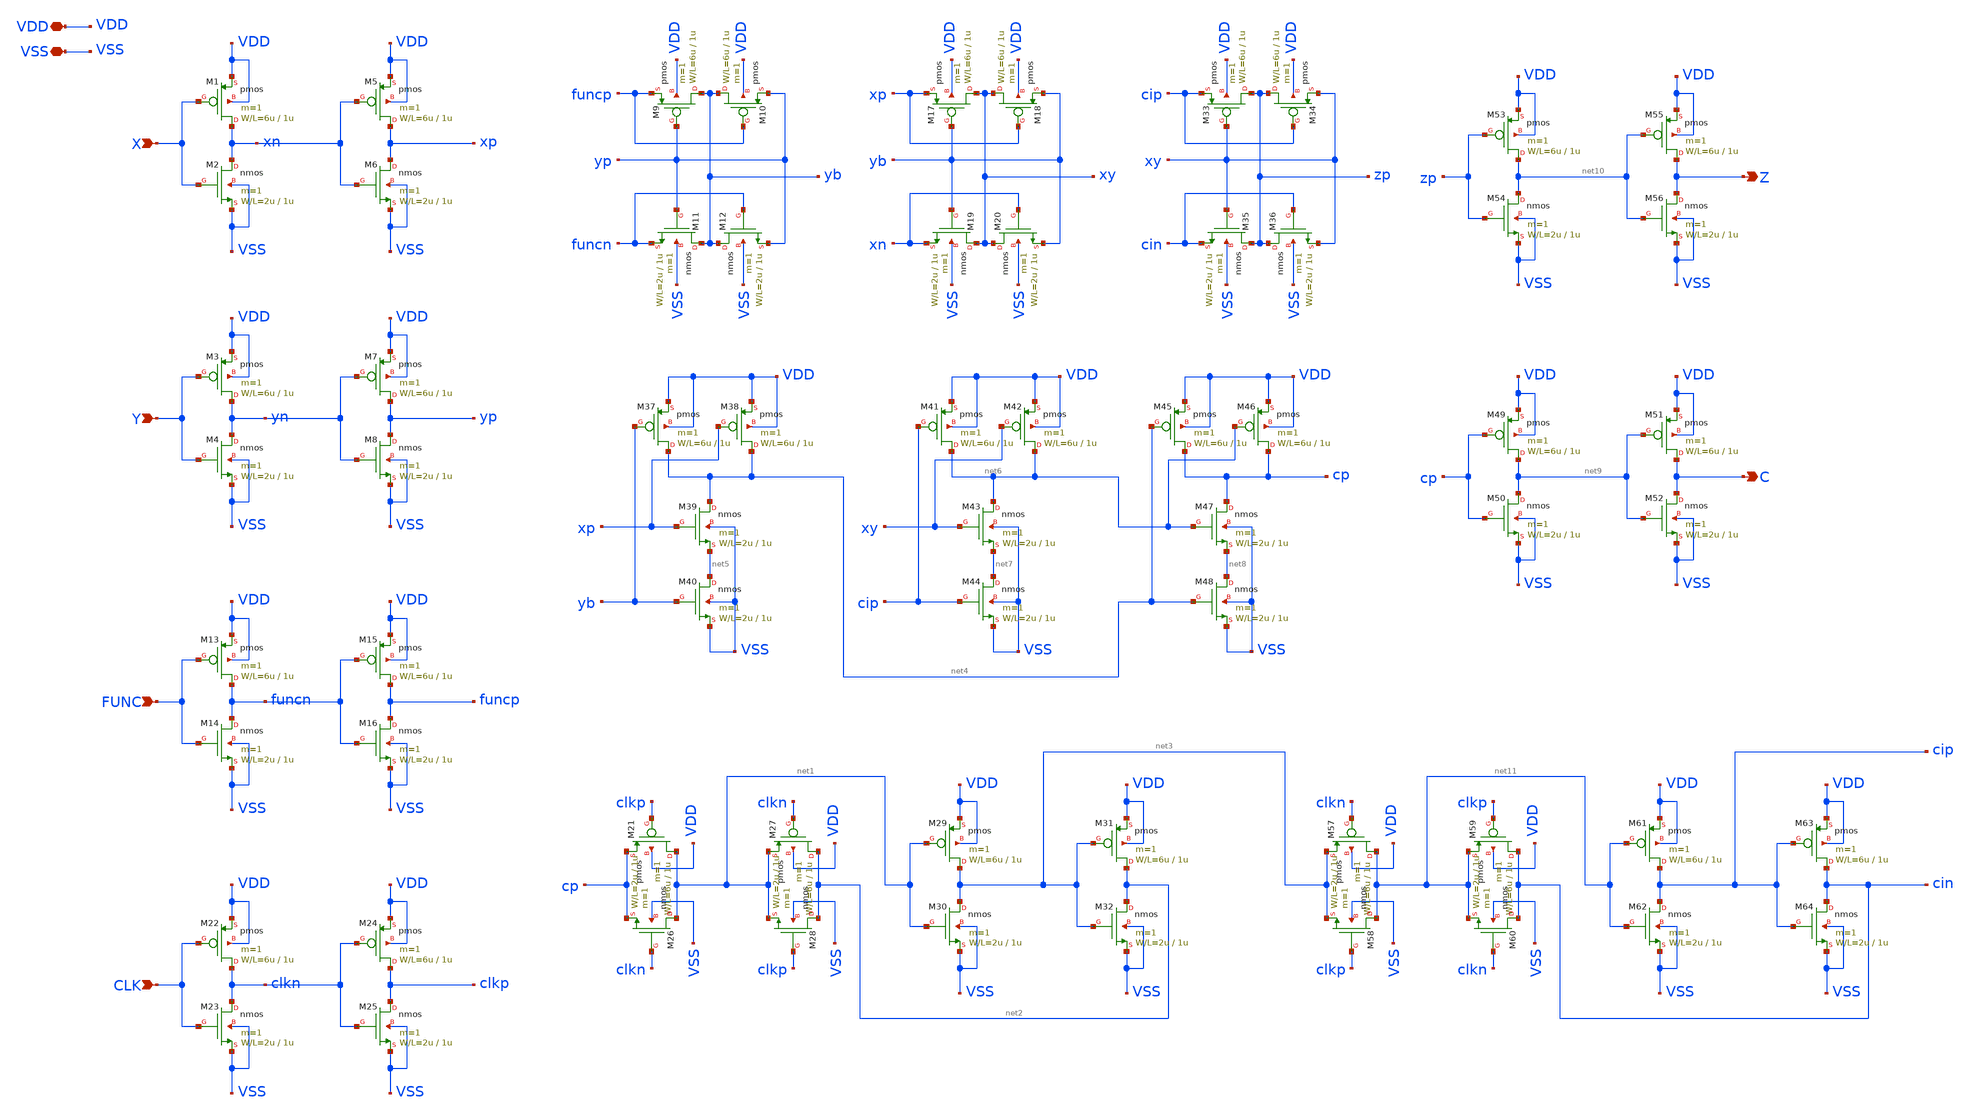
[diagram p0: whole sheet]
** sch_path: member_project/sanken/yamazaki/infinite_ALU/infinite_ALU.sch
**.subckt infinite_ALU X Y FUNC CLK Z C VDD VSS
*.ipin X
*.ipin Y
*.ipin FUNC
*.ipin CLK
*.opin Z
*.opin C
*.iopin VDD
*.iopin VSS
M1 xn X VDD VDD pmos L=1u W=6u m=1
M2 xn X VSS VSS nmos L=1u W=2u m=1
M3 yn Y VDD VDD pmos L=1u W=6u m=1
M4 yn Y VSS VSS nmos L=1u W=2u m=1
M5 xp xn VDD VDD pmos L=1u W=6u m=1
M6 xp xn VSS VSS nmos L=1u W=2u m=1
M7 yp yn VDD VDD pmos L=1u W=6u m=1
M8 yp yn VSS VSS nmos L=1u W=2u m=1
M9 yb yp funcp VDD pmos L=1u W=6u m=1
M10 yb funcp yp VDD pmos L=1u W=6u m=1
M11 yb yp funcn VSS nmos L=1u W=2u m=1
M12 yb funcn yp VSS nmos L=1u W=2u m=1
M13 funcn FUNC VDD VDD pmos L=1u W=6u m=1
M14 funcn FUNC VSS VSS nmos L=1u W=2u m=1
M15 funcp funcn VDD VDD pmos L=1u W=6u m=1
M16 funcp funcn VSS VSS nmos L=1u W=2u m=1
M17 xy yb xp VDD pmos L=1u W=6u m=1
M18 xy xp yb VDD pmos L=1u W=6u m=1
M19 xy yb xn VSS nmos L=1u W=2u m=1
M20 xy xn yb VSS nmos L=1u W=2u m=1
M21 net1 clkp cp VDD pmos L=1u W=6u m=1
M22 clkn CLK VDD VDD pmos L=1u W=6u m=1
M23 clkn CLK VSS VSS nmos L=1u W=2u m=1
M24 clkp clkn VDD VDD pmos L=1u W=6u m=1
M25 clkp clkn VSS VSS nmos L=1u W=2u m=1
M26 net1 clkn cp VSS nmos L=1u W=2u m=1
M27 net2 clkn net1 VDD pmos L=1u W=6u m=1
M28 net2 clkp net1 VSS nmos L=1u W=2u m=1
M29 net3 net1 VDD VDD pmos L=1u W=6u m=1
M30 net3 net1 VSS VSS nmos L=1u W=2u m=1
M31 net2 net3 VDD VDD pmos L=1u W=6u m=1
M32 net2 net3 VSS VSS nmos L=1u W=2u m=1
M33 zp xy cip VDD pmos L=1u W=6u m=1
M34 zp cip xy VDD pmos L=1u W=6u m=1
M35 zp xy cin VSS nmos L=1u W=2u m=1
M36 zp cin xy VSS nmos L=1u W=2u m=1
M37 net4 yb VDD VDD pmos L=1u W=6u m=1
M38 net4 xp VDD VDD pmos L=1u W=6u m=1
M39 net4 xp net5 VSS nmos L=1u W=2u m=1
M40 net5 yb VSS VSS nmos L=1u W=2u m=1
M41 net6 cip VDD VDD pmos L=1u W=6u m=1
M42 net6 xy VDD VDD pmos L=1u W=6u m=1
M43 net6 xy net7 VSS nmos L=1u W=2u m=1
M44 net7 cip VSS VSS nmos L=1u W=2u m=1
M45 cp net4 VDD VDD pmos L=1u W=6u m=1
M46 cp net6 VDD VDD pmos L=1u W=6u m=1
M47 cp net6 net8 VSS nmos L=1u W=2u m=1
M48 net8 net4 VSS VSS nmos L=1u W=2u m=1
M49 net9 cp VDD VDD pmos L=1u W=6u m=1
M50 net9 cp VSS VSS nmos L=1u W=2u m=1
M51 C net9 VDD VDD pmos L=1u W=6u m=1
M52 C net9 VSS VSS nmos L=1u W=2u m=1
M53 net10 zp VDD VDD pmos L=1u W=6u m=1
M54 net10 zp VSS VSS nmos L=1u W=2u m=1
M55 Z net10 VDD VDD pmos L=1u W=6u m=1
M56 Z net10 VSS VSS nmos L=1u W=2u m=1
M57 net11 clkn net3 VDD pmos L=1u W=6u m=1
M58 net11 clkp net3 VSS nmos L=1u W=2u m=1
M59 cin clkp net11 VDD pmos L=1u W=6u m=1
M60 cin clkn net11 VSS nmos L=1u W=2u m=1
M61 cip net11 VDD VDD pmos L=1u W=6u m=1
M62 cip net11 VSS VSS nmos L=1u W=2u m=1
M63 cin cip VDD VDD pmos L=1u W=6u m=1
M64 cin cip VSS VSS nmos L=1u W=2u m=1
**.ends
.end
